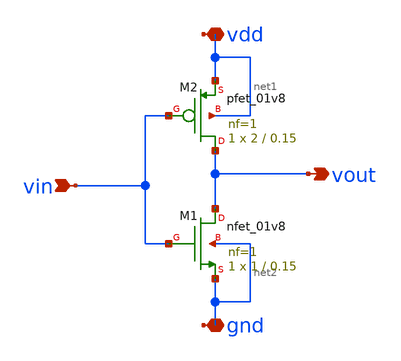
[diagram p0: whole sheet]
** sch_path: LogicGates/inverter.sch
**.subckt inverter vin vout vdd gnd
*.ipin vin
*.opin vout
*.iopin vdd
*.iopin gnd
XM1 vout vin net2 net2 sky130_fd_pr__nfet_01v8 L=0.15 W=1 nf=1 ad='int((nf+1)/2) * W/nf * 0.29' as='int((nf+2)/2) * W/nf * 0.29'
+ pd='2*int((nf+1)/2) * (W/nf + 0.29)' ps='2*int((nf+2)/2) * (W/nf + 0.29)' nrd='0.29 / W' nrs='0.29 / W'
+ sa=0 sb=0 sd=0 mult=1 m=1
XM2 vout vin net1 net1 sky130_fd_pr__pfet_01v8 L=0.15 W=2 nf=1 ad='int((nf+1)/2) * W/nf * 0.29' as='int((nf+2)/2) * W/nf * 0.29'
+ pd='2*int((nf+1)/2) * (W/nf + 0.29)' ps='2*int((nf+2)/2) * (W/nf + 0.29)' nrd='0.29 / W' nrs='0.29 / W'
+ sa=0 sb=0 sd=0 mult=1 m=1
**.ends
.end
